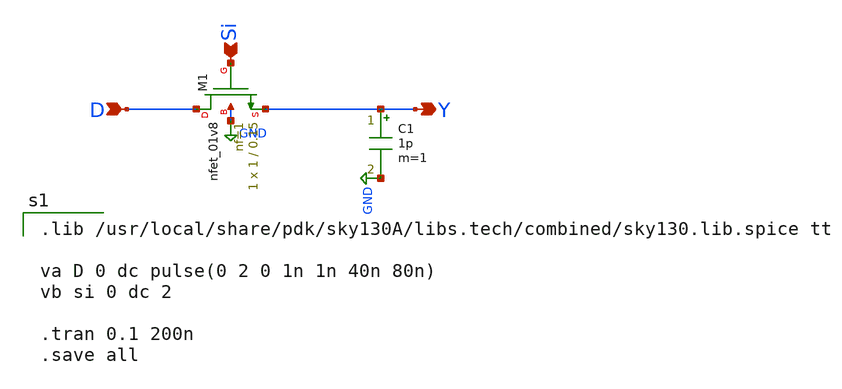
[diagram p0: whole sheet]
** sch_path: Circuit Files/circuits/first_test/untitled-5.sch
**.subckt untitled-5 D Y Si
*.ipin D
*.opin Y
*.ipin Si
C1 Y GND 1p m=1
XM1 D Si Y GND sky130_fd_pr__nfet_01v8 L=0.15 W=1 nf=1 ad='int((nf+1)/2) * W/nf * 0.29' as='int((nf+2)/2) * W/nf * 0.29'
+ pd='2*int((nf+1)/2) * (W/nf + 0.29)' ps='2*int((nf+2)/2) * (W/nf + 0.29)' nrd='0.29 / W' nrs='0.29 / W'
+ sa=0 sb=0 sd=0 mult=1 m=1
**** begin user architecture code

.lib /usr/local/share/pdk/sky130A/libs.tech/combined/sky130.lib.spice tt

va D 0 dc pulse(0 2 0 1n 1n 40n 80n)
vb si 0 dc 2

.tran 0.1 200n
.save all

**** end user architecture code
**.ends
.GLOBAL GND
.end
